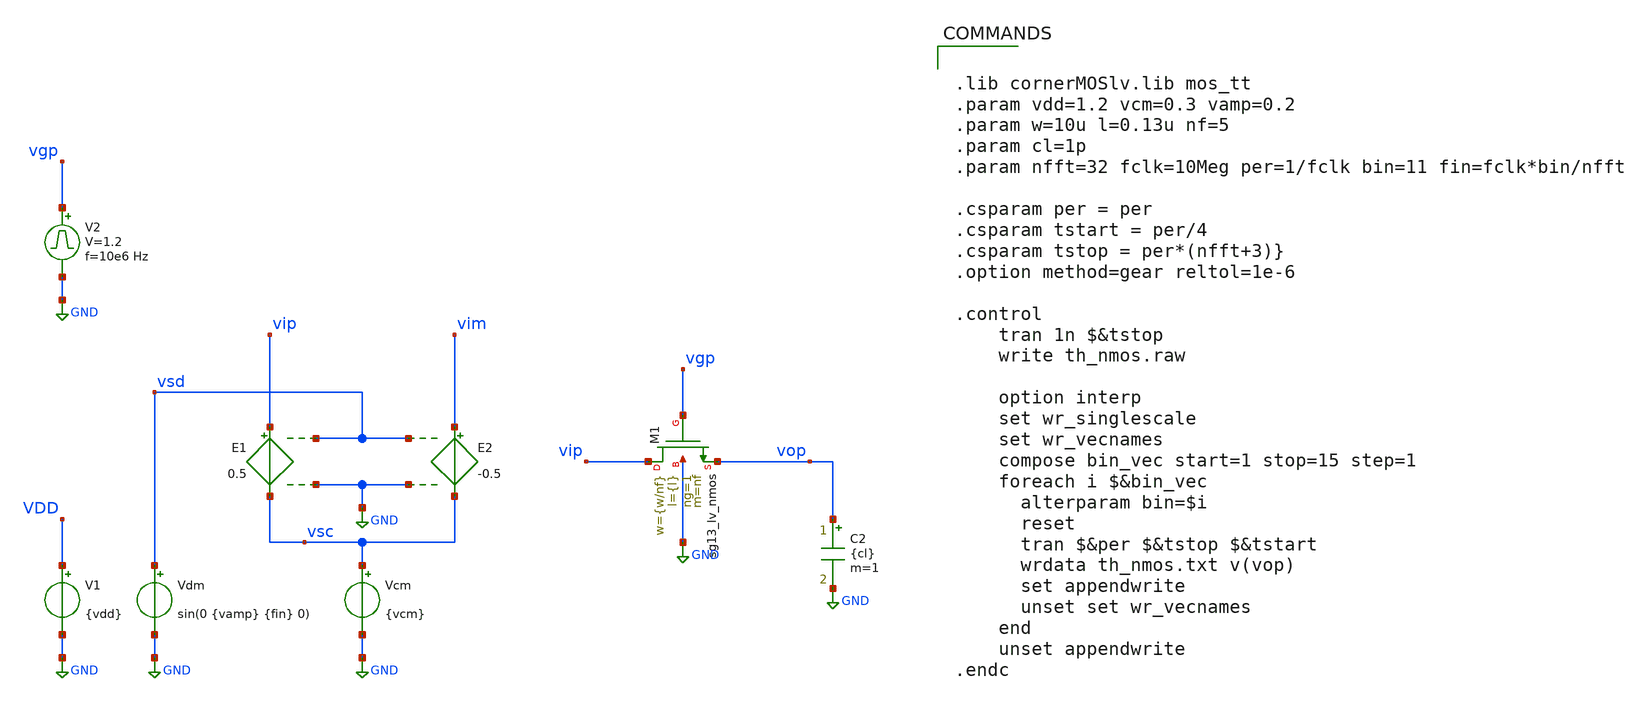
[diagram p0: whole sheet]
** sch_path: th_nmos/xschem/th_nmos.sch
**.subckt th_nmos
E1 vip vsc vsd GND 0.5
E2 vim vsc vsd GND -0.5
Vcm vsc GND {vcm}
V1 VDD GND {vdd}
XM1 vip vgp vop GND sg13_lv_nmos w={w/nf} l={l} ng=1 m=nf mm_ok=1
C2 vop GND {cl} m=1
V2 vgp GND pulse 0 1.2 '0.495/ 10e6 ' '0.01/10e6 ' '0.01/10e6 ' '0.49/10e6 ' '1/10e6 '
Vdm vsd GND sin(0 {vamp} {fin} 0)
**** begin user architecture code


.lib cornerMOSlv.lib mos_tt
.param vdd=1.2 vcm=0.3 vamp=0.2
.param w=10u l=0.13u nf=5
.param cl=1p
.param nfft=32 fclk=10Meg per=1/fclk bin=11 fin=fclk*bin/nfft

.csparam per = per
.csparam tstart = per/4
.csparam tstop = per*(nfft+3)}
.option method=gear reltol=1e-6

.control
    tran 1n $&tstop
    write th_nmos.raw

    option interp
    set wr_singlescale
    set wr_vecnames
    compose bin_vec start=1 stop=15 step=1
    foreach i $&bin_vec
      alterparam bin=$i
      reset
      tran $&per $&tstop $&tstart
      wrdata th_nmos.txt v(vop)
      set appendwrite
      unset set wr_vecnames
    end
    unset appendwrite
.endc


**** end user architecture code
**.ends
.GLOBAL GND
.end
